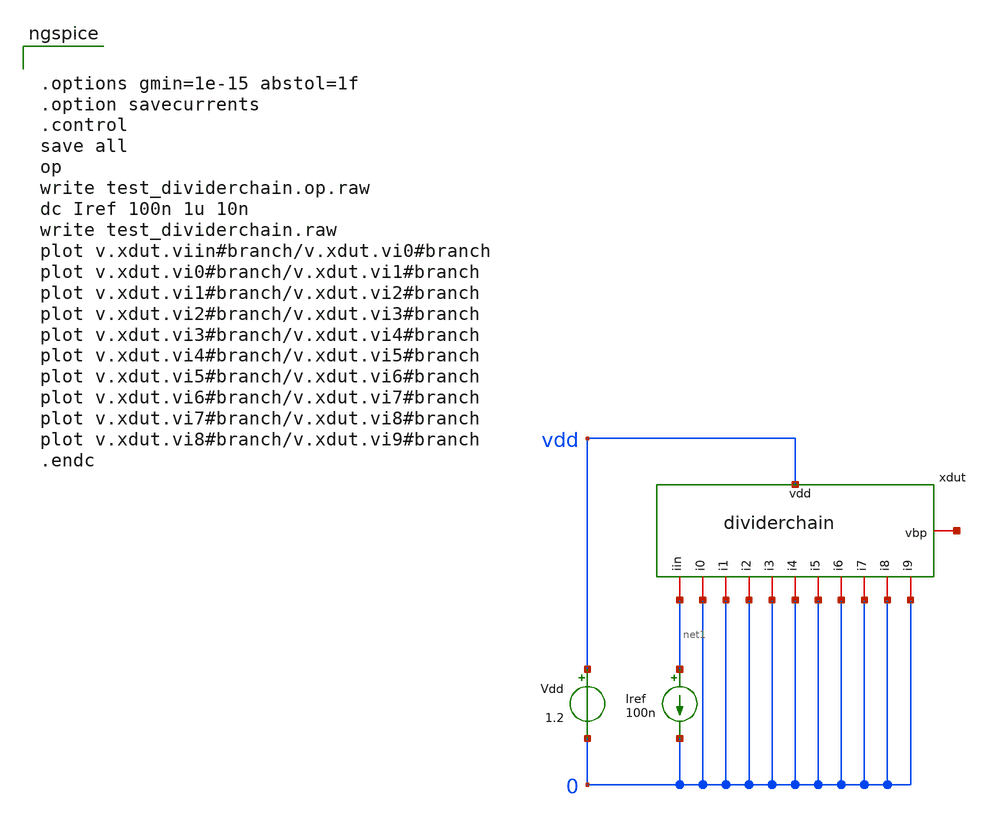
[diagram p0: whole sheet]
** sch_path: playground/test_dividerchain.sch
**.subckt test_dividerchain
xdut vdd net2 net1 0 0 0 0 0 0 0 0 0 0 dividerchain
Vdd vdd 0 1.2
Iref net1 0 100n
**** begin user architecture code

.include $::SKYWATER_MODELS/cells/nfet_01v8/sky130_fd_pr__nfet_01v8__tt.corner.spice
.include $::SKYWATER_MODELS/cells/nfet_01v8_lvt/sky130_fd_pr__nfet_01v8_lvt__tt.corner.spice
.include $::SKYWATER_MODELS/cells/pfet_01v8/sky130_fd_pr__pfet_01v8__tt.corner.spice
.include $::SKYWATER_MODELS/cells/nfet_03v3_nvt/sky130_fd_pr__nfet_03v3_nvt__tt.corner.spice
.include $::SKYWATER_MODELS/cells/nfet_05v0_nvt/sky130_fd_pr__nfet_05v0_nvt__tt.corner.spice
.include $::SKYWATER_MODELS/cells/esd_nfet_01v8/sky130_fd_pr__esd_nfet_01v8__tt.corner.spice
.include $::SKYWATER_MODELS/cells/pfet_01v8_lvt/sky130_fd_pr__pfet_01v8_lvt__tt.corner.spice
.include $::SKYWATER_MODELS/cells/pfet_01v8_hvt/sky130_fd_pr__pfet_01v8_hvt__tt.corner.spice
.include $::SKYWATER_MODELS/cells/esd_pfet_g5v0d10v5/sky130_fd_pr__esd_pfet_g5v0d10v5__tt.corner.spice
.include $::SKYWATER_MODELS/cells/pfet_g5v0d10v5/sky130_fd_pr__pfet_g5v0d10v5__tt.corner.spice
.include $::SKYWATER_MODELS/cells/pfet_g5v0d16v0/sky130_fd_pr__pfet_g5v0d16v0__tt.corner.spice
.include $::SKYWATER_MODELS/cells/nfet_g5v0d10v5/sky130_fd_pr__nfet_g5v0d10v5__tt.corner.spice
.include $::SKYWATER_MODELS/cells/nfet_g5v0d16v0/sky130_fd_pr__nfet_g5v0d16v0__tt_discrete.corner.spice
.include $::SKYWATER_MODELS/cells/esd_nfet_g5v0d10v5/sky130_fd_pr__esd_nfet_g5v0d10v5__tt.corner.spice
.include $::SKYWATER_MODELS/models/corners/tt/nonfet.spice
* Mismatch parameters
.include $::SKYWATER_MODELS/cells/nfet_01v8/sky130_fd_pr__nfet_01v8__mismatch.corner.spice
.include $::SKYWATER_MODELS/cells/pfet_01v8/sky130_fd_pr__pfet_01v8__mismatch.corner.spice
.include $::SKYWATER_MODELS/cells/nfet_01v8_lvt/sky130_fd_pr__nfet_01v8_lvt__mismatch.corner.spice
.include $::SKYWATER_MODELS/cells/pfet_01v8_lvt/sky130_fd_pr__pfet_01v8_lvt__mismatch.corner.spice
.include $::SKYWATER_MODELS/cells/pfet_01v8_hvt/sky130_fd_pr__pfet_01v8_hvt__mismatch.corner.spice
.include $::SKYWATER_MODELS/cells/nfet_g5v0d10v5/sky130_fd_pr__nfet_g5v0d10v5__mismatch.corner.spice
.include $::SKYWATER_MODELS/cells/pfet_g5v0d10v5/sky130_fd_pr__pfet_g5v0d10v5__mismatch.corner.spice
.include $::SKYWATER_MODELS/cells/nfet_05v0_nvt/sky130_fd_pr__nfet_05v0_nvt__mismatch.corner.spice
.include $::SKYWATER_MODELS/cells/nfet_03v3_nvt/sky130_fd_pr__nfet_03v3_nvt__mismatch.corner.spice
* Resistor$::SKYWATER_MODELS/Capacitor
.include $::SKYWATER_MODELS/models/r+c/res_typical__cap_typical.spice
.include $::SKYWATER_MODELS/models/r+c/res_typical__cap_typical__lin.spice
* Special cells
.include $::SKYWATER_MODELS/models/corners/tt/specialized_cells.spice
* All models
.include $::SKYWATER_MODELS/models/all.spice
* Corner
.include $::SKYWATER_MODELS/models/corners/tt/rf.spice



.options gmin=1e-15 abstol=1f
.option savecurrents
.control
save all
op
write test_dividerchain.op.raw
dc Iref 100n 1u 10n
write test_dividerchain.raw
plot v.xdut.viin#branch/v.xdut.vi0#branch
plot v.xdut.vi0#branch/v.xdut.vi1#branch
plot v.xdut.vi1#branch/v.xdut.vi2#branch
plot v.xdut.vi2#branch/v.xdut.vi3#branch
plot v.xdut.vi3#branch/v.xdut.vi4#branch
plot v.xdut.vi4#branch/v.xdut.vi5#branch
plot v.xdut.vi5#branch/v.xdut.vi6#branch
plot v.xdut.vi6#branch/v.xdut.vi7#branch
plot v.xdut.vi7#branch/v.xdut.vi8#branch
plot v.xdut.vi8#branch/v.xdut.vi9#branch
.endc


**** end user architecture code
**.ends

* expanding   symbol:  /home/cmaier/.xschem/sky130_TAC3/playground/dividerchain.sym # of pins=13
** sym_path: playground/dividerchain.sym
** sch_path: playground/dividerchain.sch
.subckt dividerchain vdd vbp iin i0 i1 i2 i3 i4 i5 i6 i7 i8 i9
*.iopin vdd
*.iopin iin
*.iopin vbp
*.iopin i0
*.iopin i1
*.iopin i2
*.iopin i3
*.iopin i4
*.iopin i5
*.iopin i6
*.iopin i7
*.iopin i8
*.iopin i9
Viin vbp iin 0
.save i(viin)
Vi0 net18 i0 0
.save i(vi0)
Vi01 vdd net1 0
.save i(vi01)
Vi1 net2 i1 0
.save i(vi1)
Vi12 net3 net4 0
.save i(vi12)
Vi2 net5 i2 0
.save i(vi2)
Vi23 net19 net6 0
.save i(vi23)
Vi3 net7 i3 0
.save i(vi3)
Vi34 net20 net8 0
.save i(vi34)
Vi4 net9 i4 0
.save i(vi4)
Vi45 net21 net10 0
.save i(vi45)
Vi5 net11 i5 0
.save i(vi5)
Vi56 net22 net12 0
.save i(vi56)
Vi6 net13 i6 0
.save i(vi6)
Vi67 net23 net14 0
.save i(vi67)
Vi7 net15 i7 0
.save i(vi7)
Vi78 net24 net16 0
.save i(vi78)
Vi8 net17 i8 0
.save i(vi8)
Vi9 net26 i9 0
.save i(vi9)
x1 vdd net1 net3 vbp net2 divider
x2 vdd net4 net19 vbp net5 divider
x3 vdd net6 net20 vbp net7 divider
x4 vdd net8 net21 vbp net9 divider
x5 vdd net10 net22 vbp net11 divider
x6 vdd net12 net23 vbp net13 divider
x7 vdd net14 net24 vbp net15 divider
x8 vdd net16 net25 vbp net17 divider
XM1 vbp vbp vdd vdd sky130_fd_pr__pfet_01v8 L=2 W=1 nf=1 ad='int((nf+1)/2) * W/nf * 0.29' as='int((nf+2)/2) * W/nf * 0.29'
+ pd='2*int((nf+1)/2) * (W/nf + 0.29)' ps='2*int((nf+2)/2) * (W/nf + 0.29)' nrd='0.29 / W' nrs='0.29 / W'
+ sa=0 sb=0 sd=0 mult=1 m=1
XM2 net18 vbp vdd vdd sky130_fd_pr__pfet_01v8 L=2 W=1 nf=1 ad='int((nf+1)/2) * W/nf * 0.29' as='int((nf+2)/2) * W/nf * 0.29'
+ pd='2*int((nf+1)/2) * (W/nf + 0.29)' ps='2*int((nf+2)/2) * (W/nf + 0.29)' nrd='0.29 / W' nrs='0.29 / W'
+ sa=0 sb=0 sd=0 mult=1 m=1
XM3 net26 vbp net25 vdd sky130_fd_pr__pfet_01v8 L=32 W=1 nf=1 ad='int((nf+1)/2) * W/nf * 0.29' as='int((nf+2)/2) * W/nf * 0.29'
+ pd='2*int((nf+1)/2) * (W/nf + 0.29)' ps='2*int((nf+2)/2) * (W/nf + 0.29)' nrd='0.29 / W' nrs='0.29 / W'
+ sa=0 sb=0 sd=0 mult=1 m=1
.ends


* expanding   symbol:  divider.sym # of pins=5
** sym_path: playground/divider.sym
** sch_path: playground/divider.sch
.subckt divider vdd iin iout vbp isink
*.iopin iin
*.iopin vdd
*.iopin vbp
*.iopin iout
*.iopin isink
XM12 node vbp net1 vdd sky130_fd_pr__pfet_01v8 L=31 W=1 nf=1 ad='int((nf+1)/2) * W/nf * 0.29' as='int((nf+2)/2) * W/nf * 0.29'
+ pd='2*int((nf+1)/2) * (W/nf + 0.29)' ps='2*int((nf+2)/2) * (W/nf + 0.29)' nrd='0.29 / W' nrs='0.29 / W'
+ sa=0 sb=0 sd=0 mult=1 m=1
Viin iin net1 0
.save i(viin)
Viout node iout 0
.save i(viout)
XM1 net2 vbp node vdd sky130_fd_pr__pfet_01v8 L=2 W=1 nf=1 ad='int((nf+1)/2) * W/nf * 0.29' as='int((nf+2)/2) * W/nf * 0.29'
+ pd='2*int((nf+1)/2) * (W/nf + 0.29)' ps='2*int((nf+2)/2) * (W/nf + 0.29)' nrd='0.29 / W' nrs='0.29 / W'
+ sa=0 sb=0 sd=0 mult=1 m=1
Visink net2 isink 0
.save i(visink)
.ends

.end
